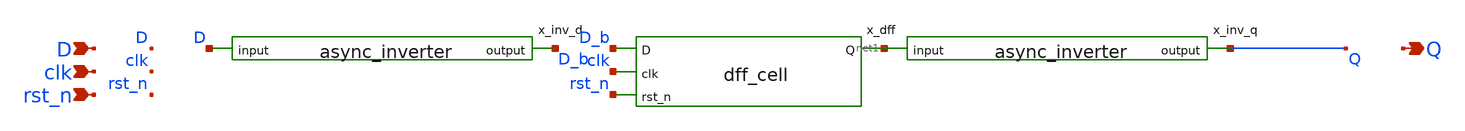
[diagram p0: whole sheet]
** sch_path: xschem/sar_adc/blocks/async_sar/dff_cell_set.sch
**.subckt dff_cell_set D clk rst_n Q
*.ipin D
*.ipin clk
*.ipin rst_n
*.opin Q
x_inv_d D D_b async_inverter
x_dff D_b clk rst_n net1 dff_cell
x_inv_q net1 Q async_inverter
**.ends

* expanding   symbol:  sar_adc/blocks/async_sar/async_inverter.sym # of pins=2
** sym_path: xschem/sar_adc/blocks/async_sar/async_inverter.sym
** sch_path: xschem/sar_adc/blocks/async_sar/async_inverter.sch
.subckt async_inverter input out
*.ipin input
*.opin out
XM5 out input VDD VDD pfet_03v3 L=0.28u W=0.80u nf=1 ad='int((nf+1)/2) * W/nf * 0.18u' as='int((nf+2)/2) * W/nf * 0.18u'
+ pd='2*int((nf+1)/2) * (W/nf + 0.18u)' ps='2*int((nf+2)/2) * (W/nf + 0.18u)' nrd='0.18u / W' nrs='0.18u / W'
+ sa=0 sb=0 sd=0 m=1
XM6 out input VSS VSS nfet_03v3 L=0.28u W=0.42u nf=1 ad='int((nf+1)/2) * W/nf * 0.18u' as='int((nf+2)/2) * W/nf * 0.18u'
+ pd='2*int((nf+1)/2) * (W/nf + 0.18u)' ps='2*int((nf+2)/2) * (W/nf + 0.18u)' nrd='0.18u / W' nrs='0.18u / W'
+ sa=0 sb=0 sd=0 m=1
.ends


* expanding   symbol:  sar_adc/blocks/async_sar/dff_cell.sym # of pins=4
** sym_path: xschem/sar_adc/dff_cell.sym
** sch_path: xschem/sar_adc/dff_cell.sch
.subckt dff_cell D clk rst_n Q
*.ipin clk
*.ipin D
*.ipin rst_n
*.opin Q
XM1 clk_n clk VDD VDD pfet_03v3 L=0.28u W=1.0u nf=1 ad='int((nf+1)/2) * W/nf * 0.18u' as='int((nf+2)/2) * W/nf * 0.18u'
+ pd='2*int((nf+1)/2) * (W/nf + 0.18u)' ps='2*int((nf+2)/2) * (W/nf + 0.18u)' nrd='0.18u / W' nrs='0.18u / W'
+ sa=0 sb=0 sd=0 m=1
XM2 clk_n clk 0 0 nfet_03v3 L=0.28u W=0.50u nf=1 ad='int((nf+1)/2) * W/nf * 0.18u' as='int((nf+2)/2) * W/nf * 0.18u'
+ pd='2*int((nf+1)/2) * (W/nf + 0.18u)' ps='2*int((nf+2)/2) * (W/nf + 0.18u)' nrd='0.18u / W' nrs='0.18u / W'
+ sa=0 sb=0 sd=0 m=1
XM3 M clk D_int VDD pfet_03v3 L=0.28u W=1.0u nf=1 ad='int((nf+1)/2) * W/nf * 0.18u' as='int((nf+2)/2) * W/nf * 0.18u'
+ pd='2*int((nf+1)/2) * (W/nf + 0.18u)' ps='2*int((nf+2)/2) * (W/nf + 0.18u)' nrd='0.18u / W' nrs='0.18u / W'
+ sa=0 sb=0 sd=0 m=1
XM4 D_int clk_n M 0 nfet_03v3 L=0.28u W=0.50u nf=1 ad='int((nf+1)/2) * W/nf * 0.18u' as='int((nf+2)/2) * W/nf * 0.18u'
+ pd='2*int((nf+1)/2) * (W/nf + 0.18u)' ps='2*int((nf+2)/2) * (W/nf + 0.18u)' nrd='0.18u / W' nrs='0.18u / W'
+ sa=0 sb=0 sd=0 m=1
XM5 M_bar M VDD VDD pfet_03v3 L=0.28u W=1.0u nf=1 ad='int((nf+1)/2) * W/nf * 0.18u' as='int((nf+2)/2) * W/nf * 0.18u'
+ pd='2*int((nf+1)/2) * (W/nf + 0.18u)' ps='2*int((nf+2)/2) * (W/nf + 0.18u)' nrd='0.18u / W' nrs='0.18u / W'
+ sa=0 sb=0 sd=0 m=1
XM6 M_bar M 0 0 nfet_03v3 L=0.28u W=0.50u nf=1 ad='int((nf+1)/2) * W/nf * 0.18u' as='int((nf+2)/2) * W/nf * 0.18u'
+ pd='2*int((nf+1)/2) * (W/nf + 0.18u)' ps='2*int((nf+2)/2) * (W/nf + 0.18u)' nrd='0.18u / W' nrs='0.18u / W'
+ sa=0 sb=0 sd=0 m=1
XM7 M M_bar VDD VDD pfet_03v3 L=2.0u W=0.30u nf=1 ad='int((nf+1)/2) * W/nf * 0.18u' as='int((nf+2)/2) * W/nf * 0.18u'
+ pd='2*int((nf+1)/2) * (W/nf + 0.18u)' ps='2*int((nf+2)/2) * (W/nf + 0.18u)' nrd='0.18u / W' nrs='0.18u / W'
+ sa=0 sb=0 sd=0 m=1
XM8 M M_bar 0 0 nfet_03v3 L=2.4u W=0.22u nf=1 ad='int((nf+1)/2) * W/nf * 0.18u' as='int((nf+2)/2) * W/nf * 0.18u'
+ pd='2*int((nf+1)/2) * (W/nf + 0.18u)' ps='2*int((nf+2)/2) * (W/nf + 0.18u)' nrd='0.18u / W' nrs='0.18u / W'
+ sa=0 sb=0 sd=0 m=1
XM9 S clk_n M_bar VDD pfet_03v3 L=0.28u W=1.0u nf=1 ad='int((nf+1)/2) * W/nf * 0.18u' as='int((nf+2)/2) * W/nf * 0.18u'
+ pd='2*int((nf+1)/2) * (W/nf + 0.18u)' ps='2*int((nf+2)/2) * (W/nf + 0.18u)' nrd='0.18u / W' nrs='0.18u / W'
+ sa=0 sb=0 sd=0 m=1
XM10 M_bar clk S 0 nfet_03v3 L=0.28u W=0.50u nf=1 ad='int((nf+1)/2) * W/nf * 0.18u' as='int((nf+2)/2) * W/nf * 0.18u'
+ pd='2*int((nf+1)/2) * (W/nf + 0.18u)' ps='2*int((nf+2)/2) * (W/nf + 0.18u)' nrd='0.18u / W' nrs='0.18u / W'
+ sa=0 sb=0 sd=0 m=1
XM11 Q_bar S VDD VDD pfet_03v3 L=0.28u W=1.0u nf=1 ad='int((nf+1)/2) * W/nf * 0.18u' as='int((nf+2)/2) * W/nf * 0.18u'
+ pd='2*int((nf+1)/2) * (W/nf + 0.18u)' ps='2*int((nf+2)/2) * (W/nf + 0.18u)' nrd='0.18u / W' nrs='0.18u / W'
+ sa=0 sb=0 sd=0 m=1
XM12 Q_bar rst_n VDD VDD pfet_03v3 L=0.28u W=1.0u nf=1 ad='int((nf+1)/2) * W/nf * 0.18u' as='int((nf+2)/2) * W/nf * 0.18u'
+ pd='2*int((nf+1)/2) * (W/nf + 0.18u)' ps='2*int((nf+2)/2) * (W/nf + 0.18u)' nrd='0.18u / W' nrs='0.18u / W'
+ sa=0 sb=0 sd=0 m=1
XM13 Q_bar S net1 0 nfet_03v3 L=0.28u W=0.50u nf=1 ad='int((nf+1)/2) * W/nf * 0.18u' as='int((nf+2)/2) * W/nf * 0.18u'
+ pd='2*int((nf+1)/2) * (W/nf + 0.18u)' ps='2*int((nf+2)/2) * (W/nf + 0.18u)' nrd='0.18u / W' nrs='0.18u / W'
+ sa=0 sb=0 sd=0 m=1
XM14 net1 rst_n 0 0 nfet_03v3 L=0.28u W=0.50u nf=1 ad='int((nf+1)/2) * W/nf * 0.18u' as='int((nf+2)/2) * W/nf * 0.18u'
+ pd='2*int((nf+1)/2) * (W/nf + 0.18u)' ps='2*int((nf+2)/2) * (W/nf + 0.18u)' nrd='0.18u / W' nrs='0.18u / W'
+ sa=0 sb=0 sd=0 m=1
XM15 Q Q_bar VDD VDD pfet_03v3 L=0.28u W=1.0u nf=1 ad='int((nf+1)/2) * W/nf * 0.18u' as='int((nf+2)/2) * W/nf * 0.18u'
+ pd='2*int((nf+1)/2) * (W/nf + 0.18u)' ps='2*int((nf+2)/2) * (W/nf + 0.18u)' nrd='0.18u / W' nrs='0.18u / W'
+ sa=0 sb=0 sd=0 m=1
XM16 Q Q_bar 0 0 nfet_03v3 L=0.28u W=0.50u nf=1 ad='int((nf+1)/2) * W/nf * 0.18u' as='int((nf+2)/2) * W/nf * 0.18u'
+ pd='2*int((nf+1)/2) * (W/nf + 0.18u)' ps='2*int((nf+2)/2) * (W/nf + 0.18u)' nrd='0.18u / W' nrs='0.18u / W'
+ sa=0 sb=0 sd=0 m=1
XM17 S Q_bar VDD VDD pfet_03v3 L=2.0u W=0.30u nf=1 ad='int((nf+1)/2) * W/nf * 0.18u' as='int((nf+2)/2) * W/nf * 0.18u'
+ pd='2*int((nf+1)/2) * (W/nf + 0.18u)' ps='2*int((nf+2)/2) * (W/nf + 0.18u)' nrd='0.18u / W' nrs='0.18u / W'
+ sa=0 sb=0 sd=0 m=1
XM18 S Q_bar 0 0 nfet_03v3 L=2.4u W=0.22u nf=1 ad='int((nf+1)/2) * W/nf * 0.18u' as='int((nf+2)/2) * W/nf * 0.18u'
+ pd='2*int((nf+1)/2) * (W/nf + 0.18u)' ps='2*int((nf+2)/2) * (W/nf + 0.18u)' nrd='0.18u / W' nrs='0.18u / W'
+ sa=0 sb=0 sd=0 m=1
XM19 D_int D VDD VDD pfet_03v3 L=0.28u W=1.0u nf=1 ad='int((nf+1)/2) * W/nf * 0.18u' as='int((nf+2)/2) * W/nf * 0.18u'
+ pd='2*int((nf+1)/2) * (W/nf + 0.18u)' ps='2*int((nf+2)/2) * (W/nf + 0.18u)' nrd='0.18u / W' nrs='0.18u / W'
+ sa=0 sb=0 sd=0 m=1
XM20 D_int D 0 0 nfet_03v3 L=0.28u W=0.50u nf=1 ad='int((nf+1)/2) * W/nf * 0.18u' as='int((nf+2)/2) * W/nf * 0.18u'
+ pd='2*int((nf+1)/2) * (W/nf + 0.18u)' ps='2*int((nf+2)/2) * (W/nf + 0.18u)' nrd='0.18u / W' nrs='0.18u / W'
+ sa=0 sb=0 sd=0 m=1
.ends

.GLOBAL VDD
.end
